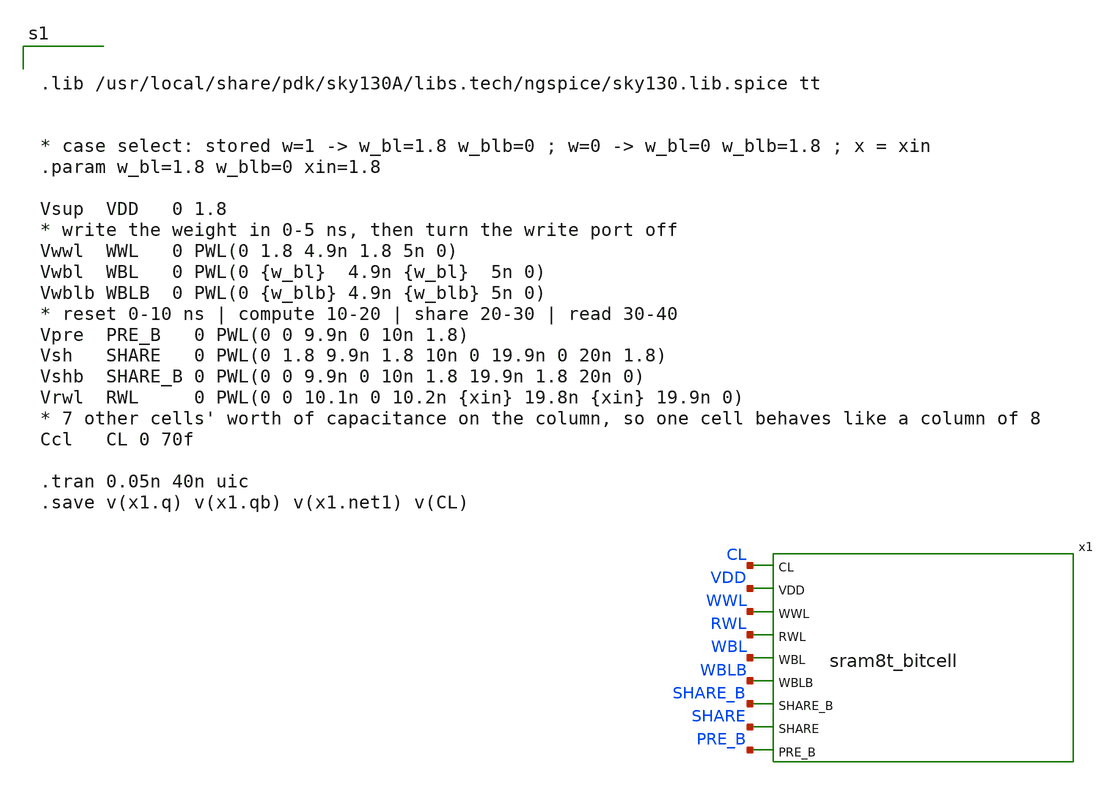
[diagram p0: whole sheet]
** sch_path: schematics/sram8t_test.sch
**.subckt sram8t_test
x1 CL VDD WWL RWL WBL WBLB SHARE_B SHARE PRE_B sram8t_bitcell
**** begin user architecture code


.lib /usr/local/share/pdk/sky130A/libs.tech/ngspice/sky130.lib.spice tt


* case select: stored w=1 -> w_bl=1.8 w_blb=0 ; w=0 -> w_bl=0 w_blb=1.8 ; x = xin
.param w_bl=1.8 w_blb=0 xin=1.8

Vsup  VDD   0 1.8
* write the weight in 0-5 ns, then turn the write port off
Vwwl  WWL   0 PWL(0 1.8 4.9n 1.8 5n 0)
Vwbl  WBL   0 PWL(0 {w_bl}  4.9n {w_bl}  5n 0)
Vwblb WBLB  0 PWL(0 {w_blb} 4.9n {w_blb} 5n 0)
* reset 0-10 ns | compute 10-20 | share 20-30 | read 30-40
Vpre  PRE_B   0 PWL(0 0 9.9n 0 10n 1.8)
Vsh   SHARE   0 PWL(0 1.8 9.9n 1.8 10n 0 19.9n 0 20n 1.8)
Vshb  SHARE_B 0 PWL(0 0 9.9n 0 10n 1.8 19.9n 1.8 20n 0)
Vrwl  RWL     0 PWL(0 0 10.1n 0 10.2n {xin} 19.8n {xin} 19.9n 0)
* 7 other cells' worth of capacitance on the column, so one cell behaves like a column of 8
Ccl   CL 0 70f

.tran 0.05n 40n uic
.save v(x1.q) v(x1.qb) v(x1.net1) v(CL)


**** end user architecture code
**.ends
.end
